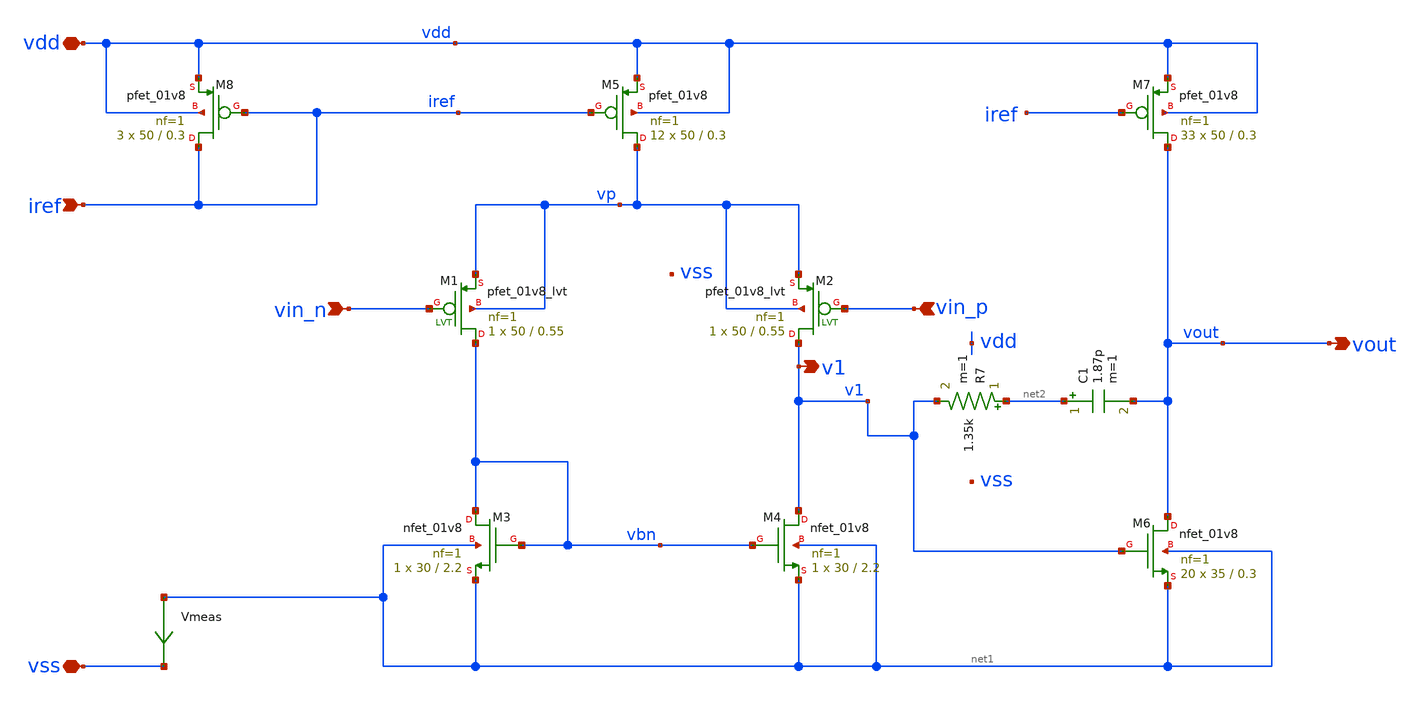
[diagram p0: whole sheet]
** sch_path: opamp/opamp.sch
**.subckt opamp vdd vss vin_n vin_p iref vout v1
*.iopin vdd
*.iopin vss
*.ipin vin_n
*.ipin vin_p
*.ipin iref
*.opin vout
*.opin v1
XM5 vp iref vdd vdd sky130_fd_pr__pfet_01v8 L=0.3 W=50 nf=1 ad='W * 0.29' as='W * 0.29' pd='2 * (W + 0.29)'
+ ps='2 * (W + 0.29)' nrd='0.29 / W' nrs='0.29 / W' sa=0 sb=0 sd=0 mult=12 m=12
XM7 vout iref vdd vdd sky130_fd_pr__pfet_01v8 L=0.3 W=50 nf=1 ad='W * 0.29' as='W * 0.29' pd='2 * (W + 0.29)'
+ ps='2 * (W + 0.29)' nrd='0.29 / W' nrs='0.29 / W' sa=0 sb=0 sd=0 mult=33 m=33
XM8 iref iref vdd vdd sky130_fd_pr__pfet_01v8 L=0.3 W=50 nf=1 ad='W * 0.29' as='W * 0.29' pd='2 * (W + 0.29)'
+ ps='2 * (W + 0.29)' nrd='0.29 / W' nrs='0.29 / W' sa=0 sb=0 sd=0 mult=3 m=3
XM1 vbn vin_n vp vp sky130_fd_pr__pfet_01v8_lvt L=0.55 W=50 nf=1 ad='int((nf+1)/2) * W/nf * 0.29' as='int((nf+2)/2) * W/nf * 0.29'
+ pd='2*int((nf+1)/2) * (W/nf + 0.29)' ps='2*int((nf+2)/2) * (W/nf + 0.29)' nrd='0.29 / W' nrs='0.29 / W'
+ sa=0 sb=0 sd=0 mult=1 m=1
XM2 v1 vin_p vp vp sky130_fd_pr__pfet_01v8_lvt L=0.55 W=50 nf=1 ad='int((nf+1)/2) * W/nf * 0.29' as='int((nf+2)/2) * W/nf * 0.29'
+ pd='2*int((nf+1)/2) * (W/nf + 0.29)' ps='2*int((nf+2)/2) * (W/nf + 0.29)' nrd='0.29 / W' nrs='0.29 / W'
+ sa=0 sb=0 sd=0 mult=1 m=1
C1 net2 vout 1.87p m=1
Vmeas net1 vss 0
.save i(vmeas)
R7 net2 v1 1.35k m=1
XM6 vout v1 net1 net1 sky130_fd_pr__nfet_01v8 L=0.3 W=35 nf=1 ad='W * 0.29' as='W * 0.29' pd='2 * (W + 0.29)'
+ ps='2 * (W + 0.29)' nrd='0.29 / W' nrs='0.29 / W' sa=0 sb=0 sd=0 mult=20 m=20
XM4 v1 vbn net1 net1 sky130_fd_pr__nfet_01v8 L=2.2 W=30 nf=1 ad='W * 0.29' as='W * 0.29' pd='2 * (W + 0.29)'
+ ps='2 * (W + 0.29)' nrd='0.29 / W' nrs='0.29 / W' sa=0 sb=0 sd=0 mult=1 m=1
XM3 vbn vbn net1 net1 sky130_fd_pr__nfet_01v8 L=2.2 W=30 nf=1 ad='W * 0.29' as='W * 0.29' pd='2 * (W + 0.29)'
+ ps='2 * (W + 0.29)' nrd='0.29 / W' nrs='0.29 / W' sa=0 sb=0 sd=0 mult=1 m=1
**.ends
.end
